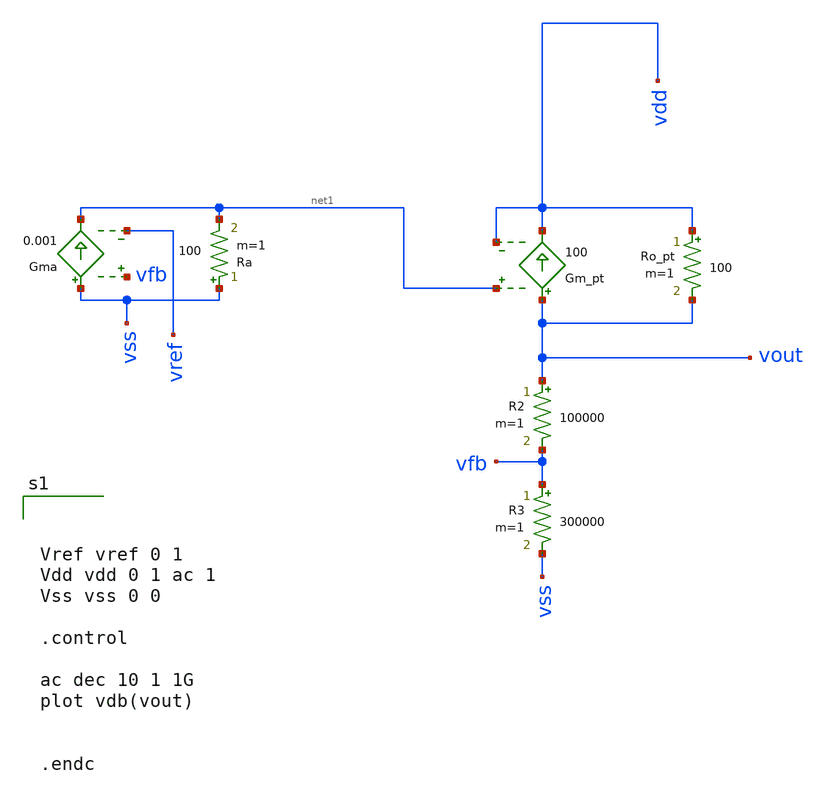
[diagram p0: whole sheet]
** sch_path: test/result_comp/xschem/ldo_tb.sch
**.subckt ldo_tb
Ro_pt vdd vout 100 m=1
Gm_pt vout vdd net1 vdd 100
R2 vout vfb 100000 m=1
R3 vfb vss 300000 m=1
Gma vss net1 vfb vref 0.001
Ra vss net1 100 m=1
**** begin user architecture code



Vref vref 0 1
Vdd vdd 0 1 ac 1
Vss vss 0 0

.control

ac dec 10 1 1G
plot vdb(vout)


.endc



**** end user architecture code
**.ends
.end
